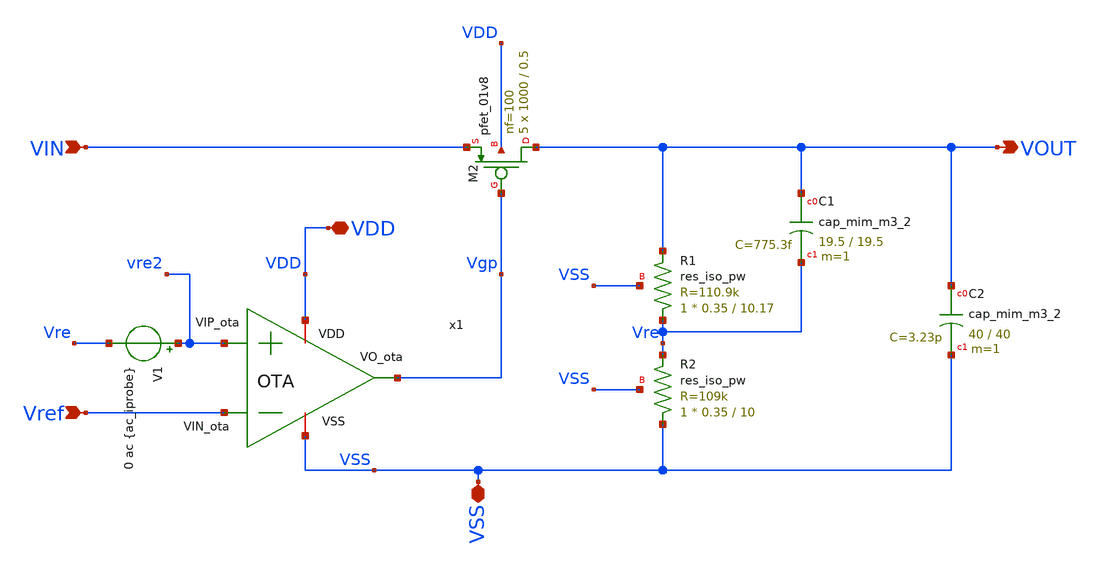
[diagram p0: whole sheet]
** sch_path: xschem/LDO.sch
**.subckt LDO VIN VDD VOUT Vref VSS
*.ipin VIN
*.iopin VDD
*.opin VOUT
*.ipin Vref
*.iopin VSS
XR1 Vre VOUT VSS sky130_fd_pr__res_iso_pw W=0.35 L=10.17 m=1
XR2 VSS Vre VSS sky130_fd_pr__res_iso_pw W=0.35 L=10 m=1
V1 vre2 Vre 0 ac {ac_iprobe}
XC1 VOUT Vre sky130_fd_pr__cap_mim_m3_2 W=19.5 L=19.5 MF=1 m=1
XC2 VOUT VSS sky130_fd_pr__cap_mim_m3_2 W=40 L=40 MF=1 m=1
x1 VDD Vgp Vref vre2 VSS OTA
XM2 VOUT Vgp VIN VDD sky130_fd_pr__pfet_01v8 L=0.5 W=1000 nf=100 ad='int((100 + 1)/2) * 1000 / 100 * 0.29'
+ as='int((100 + 2)/2) * 1000 / 100 * 0.29' pd='2*int((100 + 1)/2) * (1000 / 100 + 0.29)' ps='2*int((100 + 2)/2) * (1000 / 100 + 0.29)'
+ nrd='0.29 / 1000 ' nrs='0.29 / 1000 ' sa=0 sb=0 sd=0 mult=5 m=5
**.ends

* expanding   symbol:  /foss/designs/LDO-sky130/xschem/OTA.sym # of pins=5
** sym_path: xschem/OTA.sym
** sch_path: xschem/OTA.sch
.subckt OTA VDD VO_ota VIN_ota VIP_ota VSS
*.ipin VIN_ota
*.opin VO_ota
*.iopin VSS
*.iopin VDD
*.ipin VIP_ota
XR1 VO_ota1 net1 VDD sky130_fd_pr__res_high_po W=0.35 L=360 mult=1 m=1
XC1 VO_ota net1 sky130_fd_pr__cap_mim_m3_2 W=50 L=50 MF=1 m=1
XMpr VO_ota1 vd VSS VSS sky130_fd_pr__nfet_01v8 L=0.5 W=3 nf=1 ad='int((1 + 1)/2) * 3 / 1 * 0.29' as='int((1 + 2)/2) * 3 / 1 * 0.29'
+ pd='2*int((1 + 1)/2) * (3 / 1 + 0.29)' ps='2*int((1 + 2)/2) * (3 / 1 + 0.29)' nrd='0.29 / 3 ' nrs='0.29 / 3 '
+ sa=0 sb=0 sd=0 mult=1 m=1
XMnr vd vd VSS VSS sky130_fd_pr__nfet_01v8 L=0.5 W=3 nf=1 ad='int((1 + 1)/2) * 3 / 1 * 0.29' as='int((1 + 2)/2) * 3 / 1 * 0.29'
+ pd='2*int((1 + 1)/2) * (3 / 1 + 0.29)' ps='2*int((1 + 2)/2) * (3 / 1 + 0.29)' nrd='0.29 / 3 ' nrs='0.29 / 3 '
+ sa=0 sb=0 sd=0 mult=1 m=1
XMn vd VIN_ota Vtail VDD sky130_fd_pr__pfet_01v8 L=0.5 W=28 nf=1 ad='int((1 + 1)/2) * 28 / 1 * 0.29'
+ as='int((1 + 2)/2) * 28 / 1 * 0.29' pd='2*int((1 + 1)/2) * (28 / 1 + 0.29)' ps='2*int((1 + 2)/2) * (28 / 1 + 0.29)'
+ nrd='0.29 / 28 ' nrs='0.29 / 28 ' sa=0 sb=0 sd=0 mult=1 m=1
XMp VO_ota1 VIP_ota Vtail VDD sky130_fd_pr__pfet_01v8 L=0.5 W=28 nf=1 ad='int((1 + 1)/2) * 28 / 1 * 0.29'
+ as='int((1 + 2)/2) * 28 / 1 * 0.29' pd='2*int((1 + 1)/2) * (28 / 1 + 0.29)' ps='2*int((1 + 2)/2) * (28 / 1 + 0.29)'
+ nrd='0.29 / 28 ' nrs='0.29 / 28 ' sa=0 sb=0 sd=0 mult=1 m=1
XMo VO_ota VO_ota1 VSS VSS sky130_fd_pr__nfet_01v8 L=0.5 W=3 nf=1 ad='int((1 + 1)/2) * 3 / 1 * 0.29'
+ as='int((1 + 2)/2) * 3 / 1 * 0.29' pd='2*int((1 + 1)/2) * (3 / 1 + 0.29)' ps='2*int((1 + 2)/2) * (3 / 1 + 0.29)'
+ nrd='0.29 / 3 ' nrs='0.29 / 3 ' sa=0 sb=0 sd=0 mult=1 m=1
XMrc1 Vtail VGP VDD VDD sky130_fd_pr__pfet_01v8_lvt L=0.5 W=40 nf=1 ad='int((1 + 1)/2) * 40 / 1 * 0.29'
+ as='int((1 + 2)/2) * 40 / 1 * 0.29' pd='2*int((1 + 1)/2) * (40 / 1 + 0.29)' ps='2*int((1 + 2)/2) * (40 / 1 + 0.29)'
+ nrd='0.29 / 40 ' nrs='0.29 / 40 ' sa=0 sb=0 sd=0 mult=1 m=1
XMrc2 VO_ota VGP VDD VDD sky130_fd_pr__pfet_01v8_lvt L=0.5 W=8 nf=1 ad='int((1 + 1)/2) * 8 / 1 * 0.29'
+ as='int((1 + 2)/2) * 8 / 1 * 0.29' pd='2*int((1 + 1)/2) * (8 / 1 + 0.29)' ps='2*int((1 + 2)/2) * (8 / 1 + 0.29)'
+ nrd='0.29 / 8 ' nrs='0.29 / 8 ' sa=0 sb=0 sd=0 mult=1 m=1
XMc3 VGP Viref rs VSS sky130_fd_pr__nfet_01v8 L=1 W=20 nf=1 ad='int((1 + 1)/2) * 20 / 1 * 0.29' as='int((1 + 2)/2) * 20 / 1 * 0.29'
+ pd='2*int((1 + 1)/2) * (20 / 1 + 0.29)' ps='2*int((1 + 2)/2) * (20 / 1 + 0.29)' nrd='0.29 / 20 ' nrs='0.29 / 20 '
+ sa=0 sb=0 sd=0 mult=1 m=1
XMp2 Viref Viref VSS VSS sky130_fd_pr__nfet_01v8 L=1 W=5 nf=1 ad='int((1 + 1)/2) * 5 / 1 * 0.29' as='int((1 + 2)/2) * 5 / 1 * 0.29'
+ pd='2*int((1 + 1)/2) * (5 / 1 + 0.29)' ps='2*int((1 + 2)/2) * (5 / 1 + 0.29)' nrd='0.29 / 5 ' nrs='0.29 / 5 '
+ sa=0 sb=0 sd=0 mult=1 m=1
XMr VGP VGP VDD VDD sky130_fd_pr__pfet_01v8_lvt L=0.5 W=2.4 nf=1 ad='int((1 + 1)/2) * 2.4 / 1 * 0.29'
+ as='int((1 + 2)/2) * 2.4 / 1 * 0.29' pd='2*int((1 + 1)/2) * (2.4 / 1 + 0.29)' ps='2*int((1 + 2)/2) * (2.4 / 1 + 0.29)'
+ nrd='0.29 / 2.4 ' nrs='0.29 / 2.4 ' sa=0 sb=0 sd=0 mult=1 m=1
XMr1 Viref VGP VDD VDD sky130_fd_pr__pfet_01v8_lvt L=1 W=8 nf=1 ad='int((1 + 1)/2) * 8 / 1 * 0.29' as='int((1 + 2)/2) * 8 / 1 * 0.29'
+ pd='2*int((1 + 1)/2) * (8 / 1 + 0.29)' ps='2*int((1 + 2)/2) * (8 / 1 + 0.29)' nrd='0.29 / 8 ' nrs='0.29 / 8 '
+ sa=0 sb=0 sd=0 mult=1 m=1
XRs VSS rs VSS sky130_fd_pr__res_iso_pw W=0.425 L=0.35 m=1
.ends

.end
